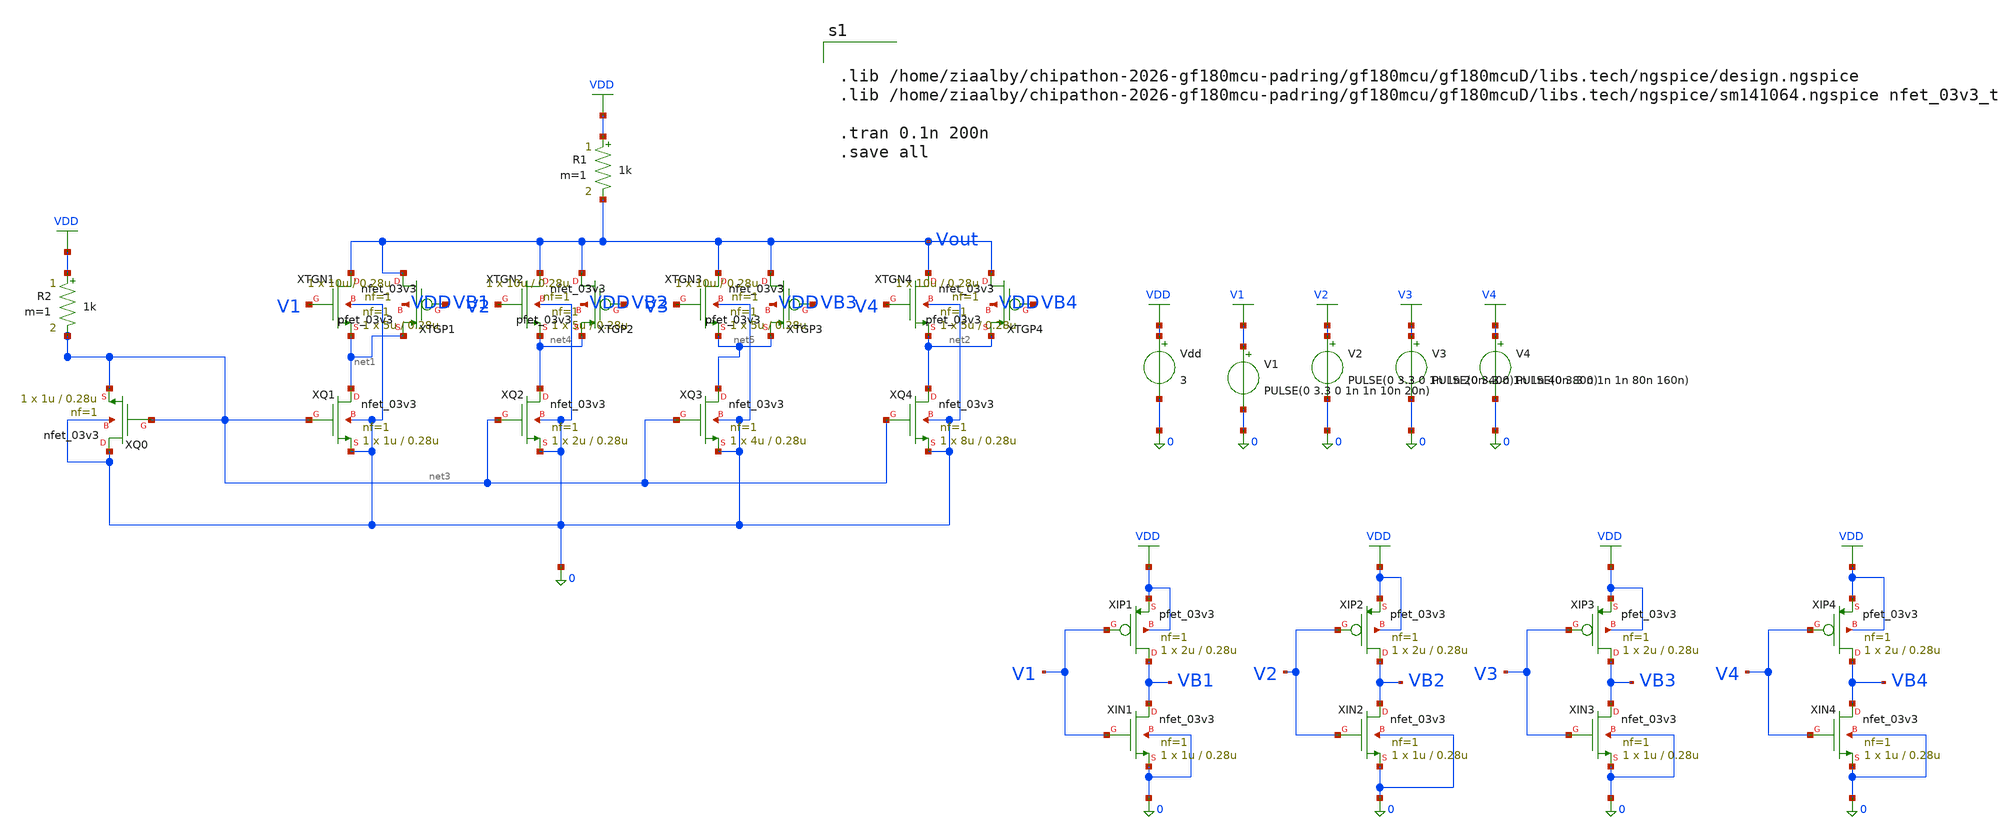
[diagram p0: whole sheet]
** sch_path: dac_tb.sch
**.subckt dac_tb
R1 VDD Vout 1k m=1
Vdd VDD 0 3
V1 V1 0 PULSE(0 3.3 0 1n 1n 10n 20n)
V2 V2 0 PULSE(0 3.3 0 1n 1n 20n 40n)
V3 V3 0 PULSE(0 3.3 0 1n 1n 40n 80n)
V4 V4 0 PULSE(0 3.3 0 1n 1n 80n 160n)
R2 VDD net3 1k m=1
XQ1 net1 net3 0 0 nfet_03v3 L=0.28u W=1u nf=1 ad='int((nf+1)/2) * W/nf * 0.18u' as='int((nf+2)/2) * W/nf * 0.18u'
+ pd='2*int((nf+1)/2) * (W/nf + 0.18u)' ps='2*int((nf+2)/2) * (W/nf + 0.18u)' nrd='0.18u / W' nrs='0.18u / W'
+ sa=0 sb=0 sd=0 m=1
XQ2 net4 net3 0 0 nfet_03v3 L=0.28u W=2u nf=1 ad='int((nf+1)/2) * W/nf * 0.18u' as='int((nf+2)/2) * W/nf * 0.18u'
+ pd='2*int((nf+1)/2) * (W/nf + 0.18u)' ps='2*int((nf+2)/2) * (W/nf + 0.18u)' nrd='0.18u / W' nrs='0.18u / W'
+ sa=0 sb=0 sd=0 m=1
XQ3 net5 net3 0 0 nfet_03v3 L=0.28u W=4u nf=1 ad='int((nf+1)/2) * W/nf * 0.18u' as='int((nf+2)/2) * W/nf * 0.18u'
+ pd='2*int((nf+1)/2) * (W/nf + 0.18u)' ps='2*int((nf+2)/2) * (W/nf + 0.18u)' nrd='0.18u / W' nrs='0.18u / W'
+ sa=0 sb=0 sd=0 m=1
XQ4 net2 net3 0 0 nfet_03v3 L=0.28u W=8u nf=1 ad='int((nf+1)/2) * W/nf * 0.18u' as='int((nf+2)/2) * W/nf * 0.18u'
+ pd='2*int((nf+1)/2) * (W/nf + 0.18u)' ps='2*int((nf+2)/2) * (W/nf + 0.18u)' nrd='0.18u / W' nrs='0.18u / W'
+ sa=0 sb=0 sd=0 m=1
XQ0 0 net3 net3 0 nfet_03v3 L=0.28u W=1u nf=1 ad='int((nf+1)/2) * W/nf * 0.18u' as='int((nf+2)/2) * W/nf * 0.18u'
+ pd='2*int((nf+1)/2) * (W/nf + 0.18u)' ps='2*int((nf+2)/2) * (W/nf + 0.18u)' nrd='0.18u / W' nrs='0.18u / W'
+ sa=0 sb=0 sd=0 m=1
XTGN1 Vout V1 net1 0 nfet_03v3 L=0.28u W=5u nf=1 ad='int((nf+1)/2) * W/nf * 0.18u' as='int((nf+2)/2) * W/nf * 0.18u'
+ pd='2*int((nf+1)/2) * (W/nf + 0.18u)' ps='2*int((nf+2)/2) * (W/nf + 0.18u)' nrd='0.18u / W' nrs='0.18u / W'
+ sa=0 sb=0 sd=0 m=1
XTGN2 Vout V2 net4 0 nfet_03v3 L=0.28u W=5u nf=1 ad='int((nf+1)/2) * W/nf * 0.18u' as='int((nf+2)/2) * W/nf * 0.18u'
+ pd='2*int((nf+1)/2) * (W/nf + 0.18u)' ps='2*int((nf+2)/2) * (W/nf + 0.18u)' nrd='0.18u / W' nrs='0.18u / W'
+ sa=0 sb=0 sd=0 m=1
XTGN3 Vout V3 net5 0 nfet_03v3 L=0.28u W=5u nf=1 ad='int((nf+1)/2) * W/nf * 0.18u' as='int((nf+2)/2) * W/nf * 0.18u'
+ pd='2*int((nf+1)/2) * (W/nf + 0.18u)' ps='2*int((nf+2)/2) * (W/nf + 0.18u)' nrd='0.18u / W' nrs='0.18u / W'
+ sa=0 sb=0 sd=0 m=1
XTGN4 Vout V4 net2 0 nfet_03v3 L=0.28u W=5u nf=1 ad='int((nf+1)/2) * W/nf * 0.18u' as='int((nf+2)/2) * W/nf * 0.18u'
+ pd='2*int((nf+1)/2) * (W/nf + 0.18u)' ps='2*int((nf+2)/2) * (W/nf + 0.18u)' nrd='0.18u / W' nrs='0.18u / W'
+ sa=0 sb=0 sd=0 m=1
XTGP1 Vout VB1 net1 VDD pfet_03v3 L=0.28u W=10u nf=1 ad='int((nf+1)/2) * W/nf * 0.18u' as='int((nf+2)/2) * W/nf * 0.18u'
+ pd='2*int((nf+1)/2) * (W/nf + 0.18u)' ps='2*int((nf+2)/2) * (W/nf + 0.18u)' nrd='0.18u / W' nrs='0.18u / W'
+ sa=0 sb=0 sd=0 m=1
XTGP2 Vout VB2 net4 VDD pfet_03v3 L=0.28u W=10u nf=1 ad='int((nf+1)/2) * W/nf * 0.18u' as='int((nf+2)/2) * W/nf * 0.18u'
+ pd='2*int((nf+1)/2) * (W/nf + 0.18u)' ps='2*int((nf+2)/2) * (W/nf + 0.18u)' nrd='0.18u / W' nrs='0.18u / W'
+ sa=0 sb=0 sd=0 m=1
XTGP3 Vout VB3 net5 VDD pfet_03v3 L=0.28u W=10u nf=1 ad='int((nf+1)/2) * W/nf * 0.18u' as='int((nf+2)/2) * W/nf * 0.18u'
+ pd='2*int((nf+1)/2) * (W/nf + 0.18u)' ps='2*int((nf+2)/2) * (W/nf + 0.18u)' nrd='0.18u / W' nrs='0.18u / W'
+ sa=0 sb=0 sd=0 m=1
XTGP4 Vout VB4 net2 VDD pfet_03v3 L=0.28u W=10u nf=1 ad='int((nf+1)/2) * W/nf * 0.18u' as='int((nf+2)/2) * W/nf * 0.18u'
+ pd='2*int((nf+1)/2) * (W/nf + 0.18u)' ps='2*int((nf+2)/2) * (W/nf + 0.18u)' nrd='0.18u / W' nrs='0.18u / W'
+ sa=0 sb=0 sd=0 m=1
XIN1 VB1 V1 0 0 nfet_03v3 L=0.28u W=1u nf=1 ad='int((nf+1)/2) * W/nf * 0.18u' as='int((nf+2)/2) * W/nf * 0.18u'
+ pd='2*int((nf+1)/2) * (W/nf + 0.18u)' ps='2*int((nf+2)/2) * (W/nf + 0.18u)' nrd='0.18u / W' nrs='0.18u / W'
+ sa=0 sb=0 sd=0 m=1
XIP1 VB1 V1 VDD VDD pfet_03v3 L=0.28u W=2u nf=1 ad='int((nf+1)/2) * W/nf * 0.18u' as='int((nf+2)/2) * W/nf * 0.18u'
+ pd='2*int((nf+1)/2) * (W/nf + 0.18u)' ps='2*int((nf+2)/2) * (W/nf + 0.18u)' nrd='0.18u / W' nrs='0.18u / W'
+ sa=0 sb=0 sd=0 m=1
XIN2 VB2 V2 0 0 nfet_03v3 L=0.28u W=1u nf=1 ad='int((nf+1)/2) * W/nf * 0.18u' as='int((nf+2)/2) * W/nf * 0.18u'
+ pd='2*int((nf+1)/2) * (W/nf + 0.18u)' ps='2*int((nf+2)/2) * (W/nf + 0.18u)' nrd='0.18u / W' nrs='0.18u / W'
+ sa=0 sb=0 sd=0 m=1
XIP2 VB2 V2 VDD VDD pfet_03v3 L=0.28u W=2u nf=1 ad='int((nf+1)/2) * W/nf * 0.18u' as='int((nf+2)/2) * W/nf * 0.18u'
+ pd='2*int((nf+1)/2) * (W/nf + 0.18u)' ps='2*int((nf+2)/2) * (W/nf + 0.18u)' nrd='0.18u / W' nrs='0.18u / W'
+ sa=0 sb=0 sd=0 m=1
XIN3 VB3 V3 0 0 nfet_03v3 L=0.28u W=1u nf=1 ad='int((nf+1)/2) * W/nf * 0.18u' as='int((nf+2)/2) * W/nf * 0.18u'
+ pd='2*int((nf+1)/2) * (W/nf + 0.18u)' ps='2*int((nf+2)/2) * (W/nf + 0.18u)' nrd='0.18u / W' nrs='0.18u / W'
+ sa=0 sb=0 sd=0 m=1
XIP3 VB3 V3 VDD VDD pfet_03v3 L=0.28u W=2u nf=1 ad='int((nf+1)/2) * W/nf * 0.18u' as='int((nf+2)/2) * W/nf * 0.18u'
+ pd='2*int((nf+1)/2) * (W/nf + 0.18u)' ps='2*int((nf+2)/2) * (W/nf + 0.18u)' nrd='0.18u / W' nrs='0.18u / W'
+ sa=0 sb=0 sd=0 m=1
XIN4 VB4 V4 0 0 nfet_03v3 L=0.28u W=1u nf=1 ad='int((nf+1)/2) * W/nf * 0.18u' as='int((nf+2)/2) * W/nf * 0.18u'
+ pd='2*int((nf+1)/2) * (W/nf + 0.18u)' ps='2*int((nf+2)/2) * (W/nf + 0.18u)' nrd='0.18u / W' nrs='0.18u / W'
+ sa=0 sb=0 sd=0 m=1
XIP4 VB4 V4 VDD VDD pfet_03v3 L=0.28u W=2u nf=1 ad='int((nf+1)/2) * W/nf * 0.18u' as='int((nf+2)/2) * W/nf * 0.18u'
+ pd='2*int((nf+1)/2) * (W/nf + 0.18u)' ps='2*int((nf+2)/2) * (W/nf + 0.18u)' nrd='0.18u / W' nrs='0.18u / W'
+ sa=0 sb=0 sd=0 m=1
**** begin user architecture code


.lib /home/ziaalby/chipathon-2026-gf180mcu-padring/gf180mcu/gf180mcuD/libs.tech/ngspice/design.ngspice
.lib /home/ziaalby/chipathon-2026-gf180mcu-padring/gf180mcu/gf180mcuD/libs.tech/ngspice/sm141064.ngspice nfet_03v3_t

.tran 0.1n 200n
.save all


**** end user architecture code
**.ends
.GLOBAL VDD
.GLOBAL V1
.GLOBAL V2
.GLOBAL V3
.GLOBAL V4
.end
